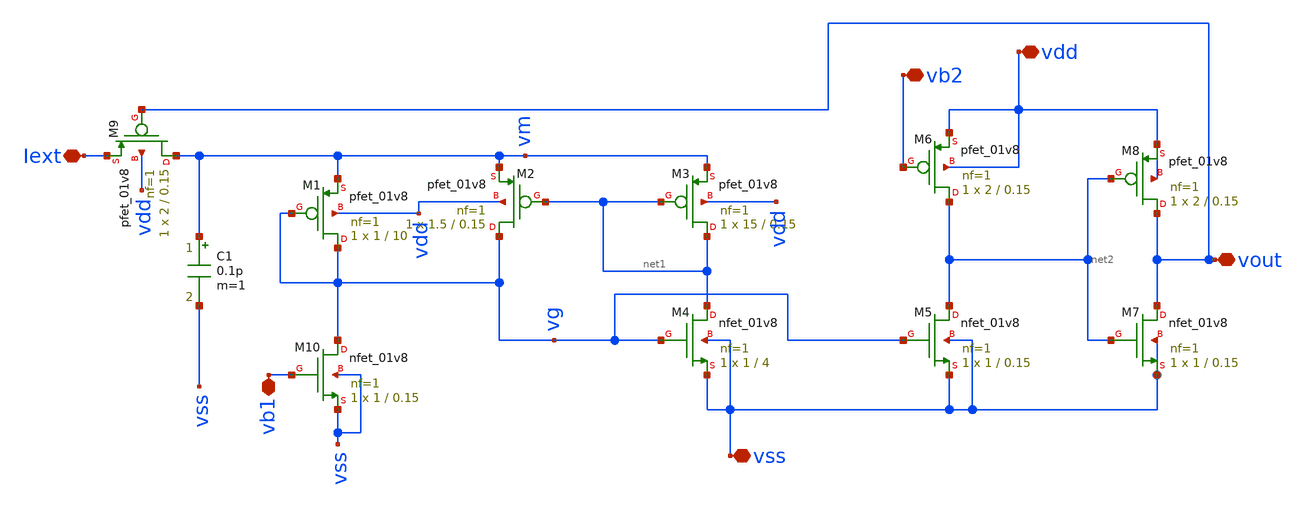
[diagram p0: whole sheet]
** sch_path: Neuron/ultralif/ul_0pF1.sch
**.subckt ul_0pF1 Iext vout vss vb1 vdd vb2
*.iopin Iext
*.iopin vout
*.iopin vss
*.iopin vb1
*.iopin vdd
*.iopin vb2
XM1 vg vg vm vdd sky130_fd_pr__pfet_01v8 L=10 W=1 nf=1 ad='int((nf+1)/2) * W/nf * 0.29' as='int((nf+2)/2) * W/nf * 0.29'
+ pd='2*int((nf+1)/2) * (W/nf + 0.29)' ps='2*int((nf+2)/2) * (W/nf + 0.29)' nrd='0.29 / W' nrs='0.29 / W'
+ sa=0 sb=0 sd=0 mult=1 m=1
XM2 vg net1 vm vdd sky130_fd_pr__pfet_01v8 L=0.15 W=1.5 nf=1 ad='int((nf+1)/2) * W/nf * 0.29' as='int((nf+2)/2) * W/nf * 0.29'
+ pd='2*int((nf+1)/2) * (W/nf + 0.29)' ps='2*int((nf+2)/2) * (W/nf + 0.29)' nrd='0.29 / W' nrs='0.29 / W'
+ sa=0 sb=0 sd=0 mult=1 m=1
XM3 net1 net1 vm vdd sky130_fd_pr__pfet_01v8 L=0.15 W=15 nf=1 ad='int((nf+1)/2) * W/nf * 0.29' as='int((nf+2)/2) * W/nf * 0.29'
+ pd='2*int((nf+1)/2) * (W/nf + 0.29)' ps='2*int((nf+2)/2) * (W/nf + 0.29)' nrd='0.29 / W' nrs='0.29 / W'
+ sa=0 sb=0 sd=0 mult=1 m=1
XM4 net1 vg vss vss sky130_fd_pr__nfet_01v8 L=4 W=1 nf=1 ad='int((1 + 1)/2) * 1 / 1 * 0.29' as='int((1 + 2)/2) * 1 / 1 * 0.29'
+ pd='2*int((1 + 1)/2) * (1 / 1 + 0.29)' ps='2*int((1 + 2)/2) * (1 / 1 + 0.29)' nrd='0.29 / 1 ' nrs='0.29 / 1 '
+ sa=0 sb=0 sd=0 mult=1 m=1
C1 vm vss 0.1p m=1
XM10 vg vb1 vss vss sky130_fd_pr__nfet_01v8 L=0.15 W=1 nf=1 ad='int((1 + 1)/2) * 1 / 1 * 0.29' as='int((1 + 2)/2) * 1 / 1 * 0.29'
+ pd='2*int((1 + 1)/2) * (1 / 1 + 0.29)' ps='2*int((1 + 2)/2) * (1 / 1 + 0.29)' nrd='0.29 / 1 ' nrs='0.29 / 1 '
+ sa=0 sb=0 sd=0 mult=1 m=1
XM5 net2 vg vss vss sky130_fd_pr__nfet_01v8 L=0.15 W=1 nf=1 ad='int((1 + 1)/2) * 1 / 1 * 0.29' as='int((1 + 2)/2) * 1 / 1 * 0.29'
+ pd='2*int((1 + 1)/2) * (1 / 1 + 0.29)' ps='2*int((1 + 2)/2) * (1 / 1 + 0.29)' nrd='0.29 / 1 ' nrs='0.29 / 1 '
+ sa=0 sb=0 sd=0 mult=1 m=1
XM6 net2 vb2 vdd vdd sky130_fd_pr__pfet_01v8 L=0.15 W=2 nf=1 ad='int((nf+1)/2) * W/nf * 0.29' as='int((nf+2)/2) * W/nf * 0.29'
+ pd='2*int((nf+1)/2) * (W/nf + 0.29)' ps='2*int((nf+2)/2) * (W/nf + 0.29)' nrd='0.29 / W' nrs='0.29 / W'
+ sa=0 sb=0 sd=0 mult=1 m=1
XM7 vout net2 vss vss sky130_fd_pr__nfet_01v8 L=0.15 W=1 nf=1 ad='int((1 + 1)/2) * 1 / 1 * 0.29' as='int((1 + 2)/2) * 1 / 1 * 0.29'
+ pd='2*int((1 + 1)/2) * (1 / 1 + 0.29)' ps='2*int((1 + 2)/2) * (1 / 1 + 0.29)' nrd='0.29 / 1 ' nrs='0.29 / 1 '
+ sa=0 sb=0 sd=0 mult=1 m=1
XM8 vout net2 vdd vdd sky130_fd_pr__pfet_01v8 L=0.15 W=2 nf=1 ad='int((nf+1)/2) * W/nf * 0.29' as='int((nf+2)/2) * W/nf * 0.29'
+ pd='2*int((nf+1)/2) * (W/nf + 0.29)' ps='2*int((nf+2)/2) * (W/nf + 0.29)' nrd='0.29 / W' nrs='0.29 / W'
+ sa=0 sb=0 sd=0 mult=1 m=1
XM9 vm vout Iext vdd sky130_fd_pr__pfet_01v8 L=0.15 W=2 nf=1 ad='int((nf+1)/2) * W/nf * 0.29' as='int((nf+2)/2) * W/nf * 0.29'
+ pd='2*int((nf+1)/2) * (W/nf + 0.29)' ps='2*int((nf+2)/2) * (W/nf + 0.29)' nrd='0.29 / W' nrs='0.29 / W'
+ sa=0 sb=0 sd=0 mult=1 m=1
**.ends
.end
